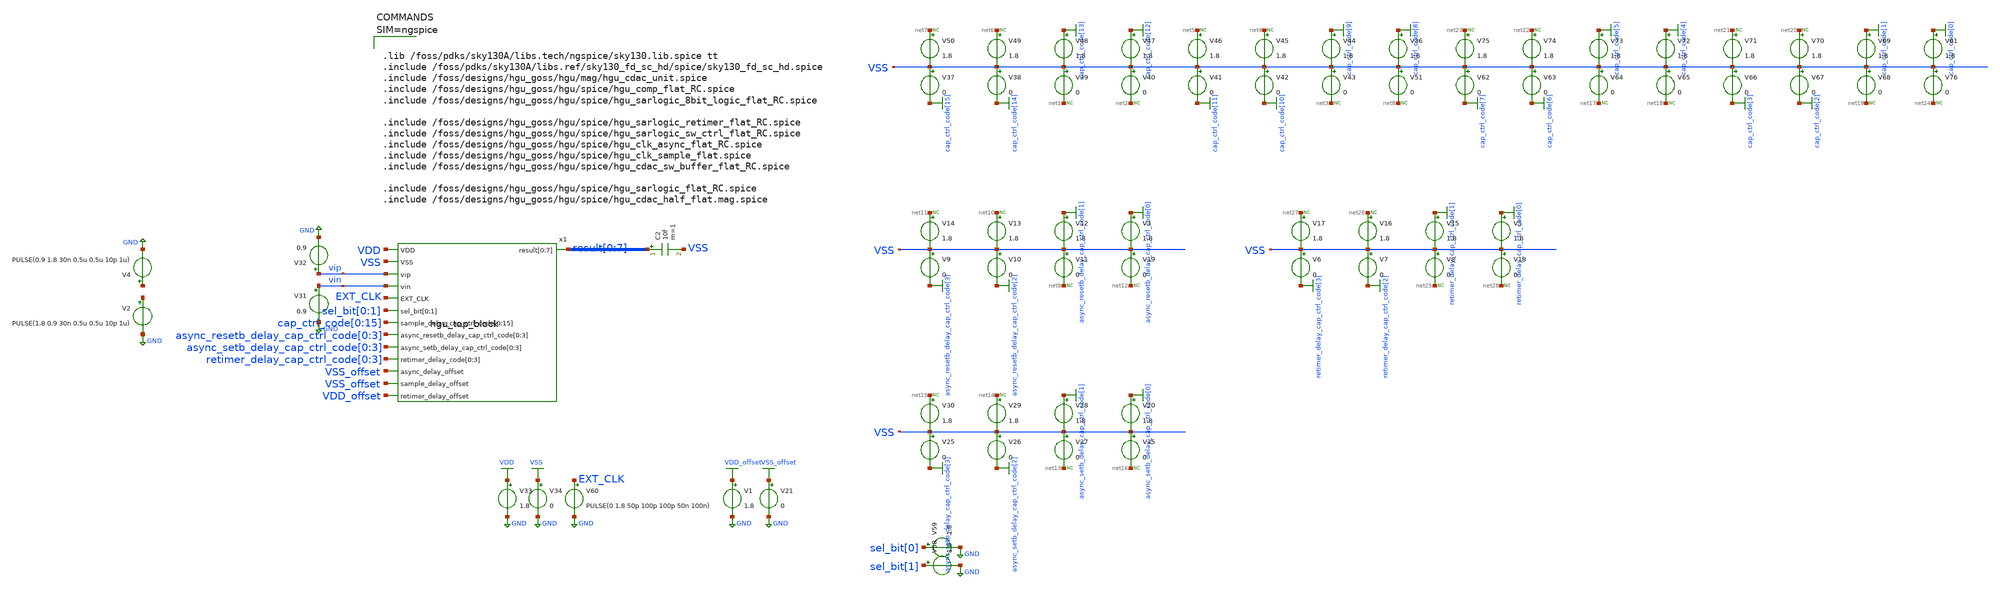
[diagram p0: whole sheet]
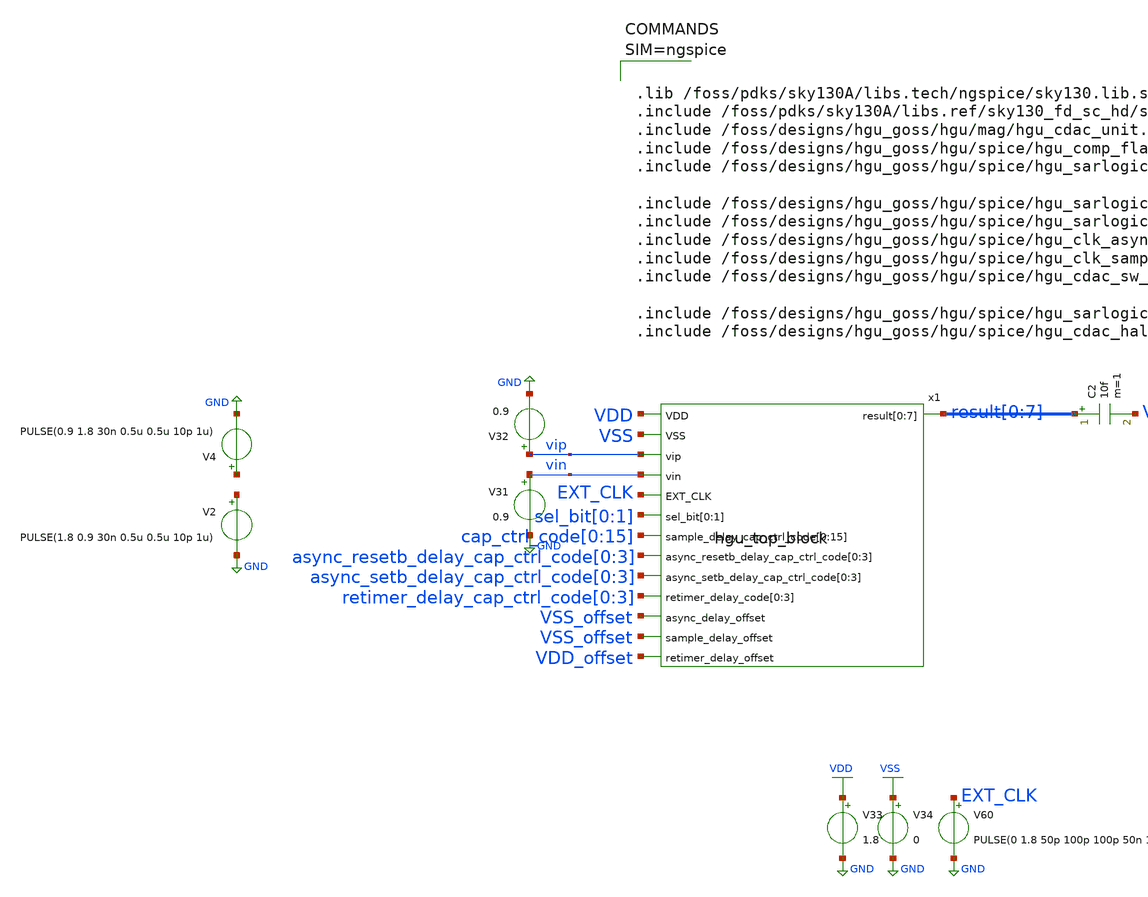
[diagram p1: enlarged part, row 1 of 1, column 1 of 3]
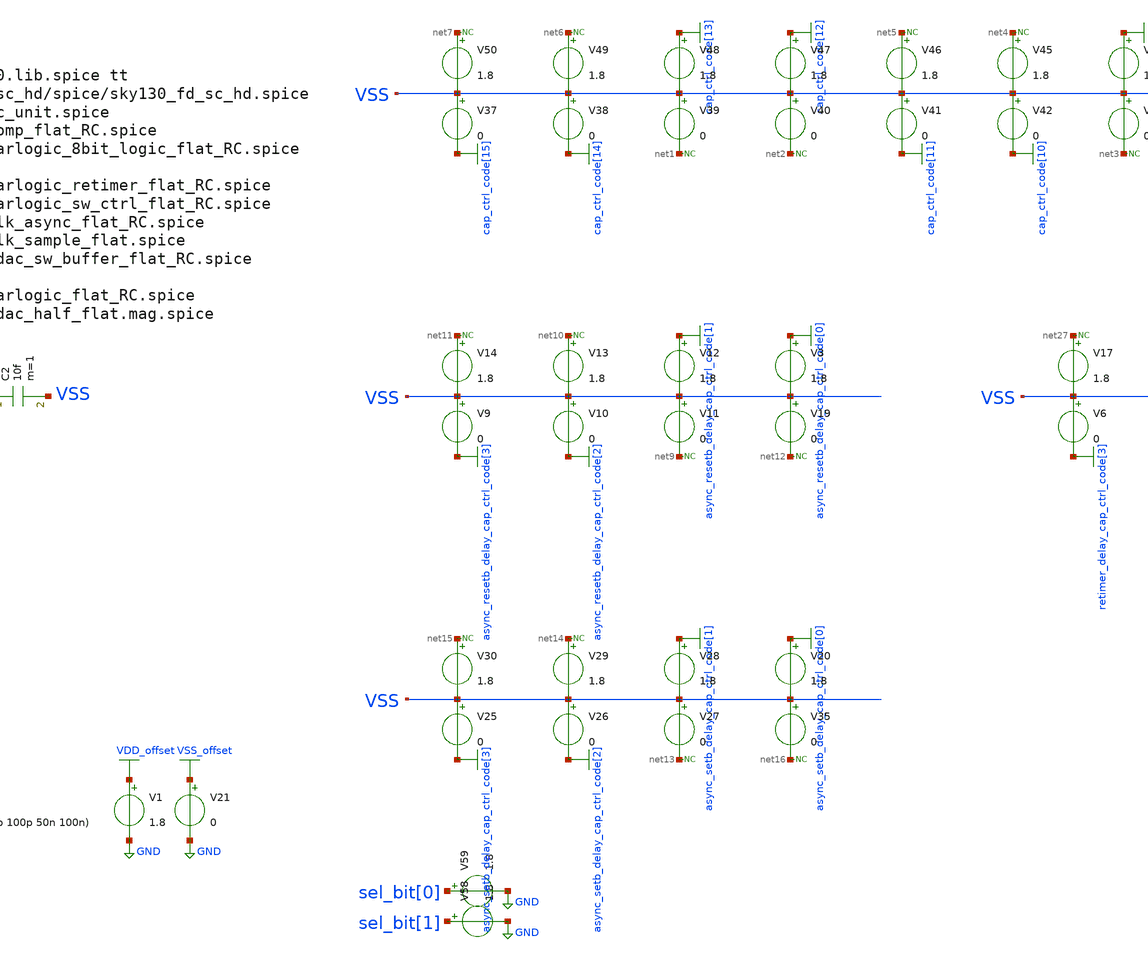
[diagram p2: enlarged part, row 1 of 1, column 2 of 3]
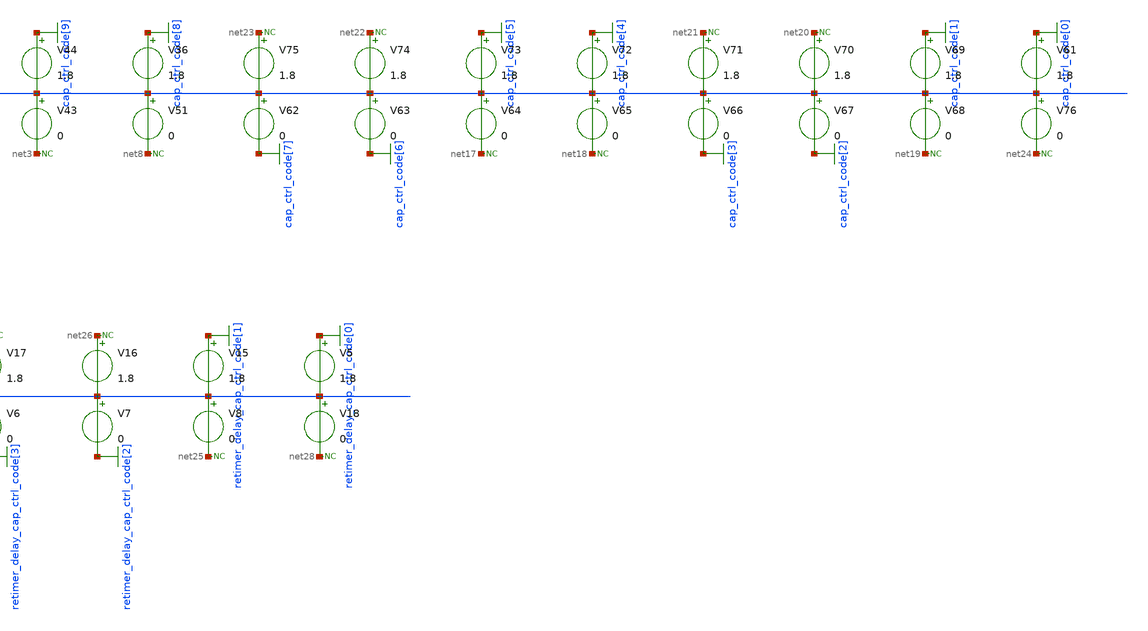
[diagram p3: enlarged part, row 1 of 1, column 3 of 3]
** sch_path: hgu/tb/tb_hgu_top_block.sch
**.subckt tb_hgu_top_block
x1 VDD result[0] result[1] result[2] result[3] result[4] result[5] result[6] result[7] VSS vip vin
+ EXT_CLK sel_bit[0] sel_bit[1] cap_ctrl_code[0] cap_ctrl_code[1] cap_ctrl_code[2] cap_ctrl_code[3]
+ cap_ctrl_code[4] cap_ctrl_code[5] cap_ctrl_code[6] cap_ctrl_code[7] cap_ctrl_code[8] cap_ctrl_code[9]
+ cap_ctrl_code[10] cap_ctrl_code[11] cap_ctrl_code[12] cap_ctrl_code[13] cap_ctrl_code[14] cap_ctrl_code[15]
+ async_resetb_delay_cap_ctrl_code[0] async_resetb_delay_cap_ctrl_code[1] async_resetb_delay_cap_ctrl_code[2]
+ async_resetb_delay_cap_ctrl_code[3] async_setb_delay_cap_ctrl_code[0] async_setb_delay_cap_ctrl_code[1]
+ async_setb_delay_cap_ctrl_code[2] async_setb_delay_cap_ctrl_code[3] retimer_delay_cap_ctrl_code[0] retimer_delay_cap_ctrl_code[1]
+ retimer_delay_cap_ctrl_code[2] retimer_delay_cap_ctrl_code[3] VSS_offset VSS_offset VDD_offset hgu_top_block
C2 result[0] VSS 10f m=1
V36 cap_ctrl_code[8] VSS 1.8
V37 VSS cap_ctrl_code[15] 0
V38 VSS cap_ctrl_code[14] 0
V39 VSS net1 0
V40 VSS net2 0
V41 VSS cap_ctrl_code[11] 0
V42 VSS cap_ctrl_code[10] 0
V43 VSS net3 0
V44 cap_ctrl_code[9] VSS 1.8
V45 net4 VSS 1.8
V46 net5 VSS 1.8
V47 cap_ctrl_code[12] VSS 1.8
V48 cap_ctrl_code[13] VSS 1.8
V49 net6 VSS 1.8
V50 net7 VSS 1.8
V51 VSS net8 0
* noconn #net7
* noconn #net6
* noconn #net1
* noconn #net2
* noconn #net5
* noconn #net4
* noconn #net3
* noconn #net8
V58 sel_bit[1] GND 1.8
V59 sel_bit[0] GND 1.8
V3 async_resetb_delay_cap_ctrl_code[0] VSS 1.8
V9 VSS async_resetb_delay_cap_ctrl_code[3] 0
V10 VSS async_resetb_delay_cap_ctrl_code[2] 0
V11 VSS net9 0
V12 async_resetb_delay_cap_ctrl_code[1] VSS 1.8
V13 net10 VSS 1.8
V14 net11 VSS 1.8
V19 VSS net12 0
* noconn #net11
* noconn #net10
* noconn #net9
* noconn #net12
V20 async_setb_delay_cap_ctrl_code[0] VSS 1.8
V25 VSS async_setb_delay_cap_ctrl_code[3] 0
V26 VSS async_setb_delay_cap_ctrl_code[2] 0
V27 VSS net13 0
V28 async_setb_delay_cap_ctrl_code[1] VSS 1.8
V29 net14 VSS 1.8
V30 net15 VSS 1.8
V35 VSS net16 0
* noconn #net15
* noconn #net14
* noconn #net13
* noconn #net16
V61 cap_ctrl_code[0] VSS 1.8
V62 VSS cap_ctrl_code[7] 0
V63 VSS cap_ctrl_code[6] 0
V64 VSS net17 0
V65 VSS net18 0
V66 VSS cap_ctrl_code[3] 0
V67 VSS cap_ctrl_code[2] 0
V68 VSS net19 0
V69 cap_ctrl_code[1] VSS 1.8
V70 net20 VSS 1.8
V71 net21 VSS 1.8
V72 cap_ctrl_code[4] VSS 1.8
V73 cap_ctrl_code[5] VSS 1.8
V74 net22 VSS 1.8
V75 net23 VSS 1.8
V76 VSS net24 0
* noconn #net23
* noconn #net22
* noconn #net17
* noconn #net18
* noconn #net21
* noconn #net20
* noconn #net19
* noconn #net24
V5 retimer_delay_cap_ctrl_code[0] VSS 1.8
V6 VSS retimer_delay_cap_ctrl_code[3] 0
V7 VSS retimer_delay_cap_ctrl_code[2] 0
V8 VSS net25 0
V15 retimer_delay_cap_ctrl_code[1] VSS 1.8
V16 net26 VSS 1.8
V17 net27 VSS 1.8
V18 VSS net28 0
* noconn #net27
* noconn #net26
* noconn #net25
* noconn #net28
V33 VDD GND 1.8
V34 VSS GND 0
V31 vin GND 0.9
V32 vip GND 0.9
V60 EXT_CLK GND PULSE(0 1.8 50p 100p 100p 50n 100n)
V2 net29 GND PULSE(1.8 0.9 30n 0.5u 0.5u 10p 1u)
V4 net30 GND PULSE(0.9 1.8 30n 0.5u 0.5u 10p 1u)
V1 VDD_offset GND 1.8
V21 VSS_offset GND 0
**** begin user architecture code



.lib /foss/pdks/sky130A/libs.tech/ngspice/sky130.lib.spice tt
.include /foss/pdks/sky130A/libs.ref/sky130_fd_sc_hd/spice/sky130_fd_sc_hd.spice
.include /foss/designs/hgu_goss/hgu/mag/hgu_cdac_unit.spice
.include /foss/designs/hgu_goss/hgu/spice/hgu_comp_flat_RC.spice
.include /foss/designs/hgu_goss/hgu/spice/hgu_sarlogic_8bit_logic_flat_RC.spice

.include /foss/designs/hgu_goss/hgu/spice/hgu_sarlogic_retimer_flat_RC.spice
.include /foss/designs/hgu_goss/hgu/spice/hgu_sarlogic_sw_ctrl_flat_RC.spice
.include /foss/designs/hgu_goss/hgu/spice/hgu_clk_async_flat_RC.spice
.include /foss/designs/hgu_goss/hgu/spice/hgu_clk_sample_flat.spice
.include /foss/designs/hgu_goss/hgu/spice/hgu_cdac_sw_buffer_flat_RC.spice

.include /foss/designs/hgu_goss/hgu/spice/hgu_sarlogic_flat_RC.spice
.include /foss/designs/hgu_goss/hgu/spice/hgu_cdac_half_flat.mag.spice






.OPTIONS savecurrents
.tran 60ps 300ns

.control
	run
	plot V(x1.sample_clk) V(vip) V(vin) V(vip)-V(vin)+0.9 V(x1.tah_vp) V(x1.tah_vn)
+ V(x1.tah_vp)-V(x1.tah_vn) V(vip)-V(vin) "result[0]"+2 "result[1]"+4 "result[2]"+6 "result[3]"+8 "result[4]"+10 "result[5]"+12
+ "result[6]"+14 "result[7]"+16


.endc
.save x1.sample_clk vip vin x1.tah_vp x1.tah_vn "result[0]" "result[1]" "result[2]" "result[3]" "result[4]" "result[5]" "result[6]" "result[7]" "x1.x1.sar_result_temp[0]" "x1.x1.sar_result_temp[1]" "x1.x1.sar_result_temp[2]" "x1.x1.sar_result_temp[3]" "x1.x1.sar_result_temp[4]" "x1.x1.sar_result_temp[5]" "x1.x1.sar_result_temp[6]" "x1.x1.sar_result_temp[7]"
.save "x1.result_sw[1]" "x1.result_sw[2]" "x1.result_sw[3]" "x1.result_sw[4]" "x1.result_sw[5]" "x1.result_sw[6]" "x1.result_sw[7]"
.save "x1.result2_sw[1]" "x1.result2_sw[2]" "x1.result2_sw[3]" "x1.result2_sw[4]" "x1.result2_sw[5]" "x1.result2_sw[6]" "x1.result2_sw[7]"
.save "x1.result_sw_b[1]" "x1.result_sw_b[2]" "x1.result_sw_b[3]" "x1.result_sw_b[4]" "x1.result_sw_b[5]" "x1.result_sw_b[6]" "x1.result_sw_b[7]"
.save "x1.result2_sw_b[1]" "x1.result2_sw_b[2]" "x1.result2_sw_b[3]" "x1.result2_sw_b[4]" "x1.result2_sw_b[5]" "x1.result2_sw_b[6]" "x1.result2_sw_b[7]"
.save x1.comp_result
.save vdd
.save v33
*.save all


**** end user architecture code
**.ends
.GLOBAL cap_ctrl_code[15]
.GLOBAL cap_ctrl_code[14]
.GLOBAL cap_ctrl_code[13]
.GLOBAL cap_ctrl_code[12]
.GLOBAL cap_ctrl_code[11]
.GLOBAL cap_ctrl_code[10]
.GLOBAL cap_ctrl_code[9]
.GLOBAL cap_ctrl_code[8]
.GLOBAL GND
.GLOBAL async_resetb_delay_cap_ctrl_code[3]
.GLOBAL async_resetb_delay_cap_ctrl_code[2]
.GLOBAL async_resetb_delay_cap_ctrl_code[1]
.GLOBAL async_resetb_delay_cap_ctrl_code[0]
.GLOBAL async_setb_delay_cap_ctrl_code[3]
.GLOBAL async_setb_delay_cap_ctrl_code[2]
.GLOBAL async_setb_delay_cap_ctrl_code[1]
.GLOBAL async_setb_delay_cap_ctrl_code[0]
.GLOBAL cap_ctrl_code[7]
.GLOBAL cap_ctrl_code[6]
.GLOBAL cap_ctrl_code[5]
.GLOBAL cap_ctrl_code[4]
.GLOBAL cap_ctrl_code[3]
.GLOBAL cap_ctrl_code[2]
.GLOBAL cap_ctrl_code[1]
.GLOBAL cap_ctrl_code[0]
.GLOBAL retimer_delay_cap_ctrl_code[3]
.GLOBAL retimer_delay_cap_ctrl_code[2]
.GLOBAL retimer_delay_cap_ctrl_code[1]
.GLOBAL retimer_delay_cap_ctrl_code[0]
.GLOBAL VDD
.GLOBAL VSS
.GLOBAL VDD_offset
.GLOBAL VSS_offset
.end
